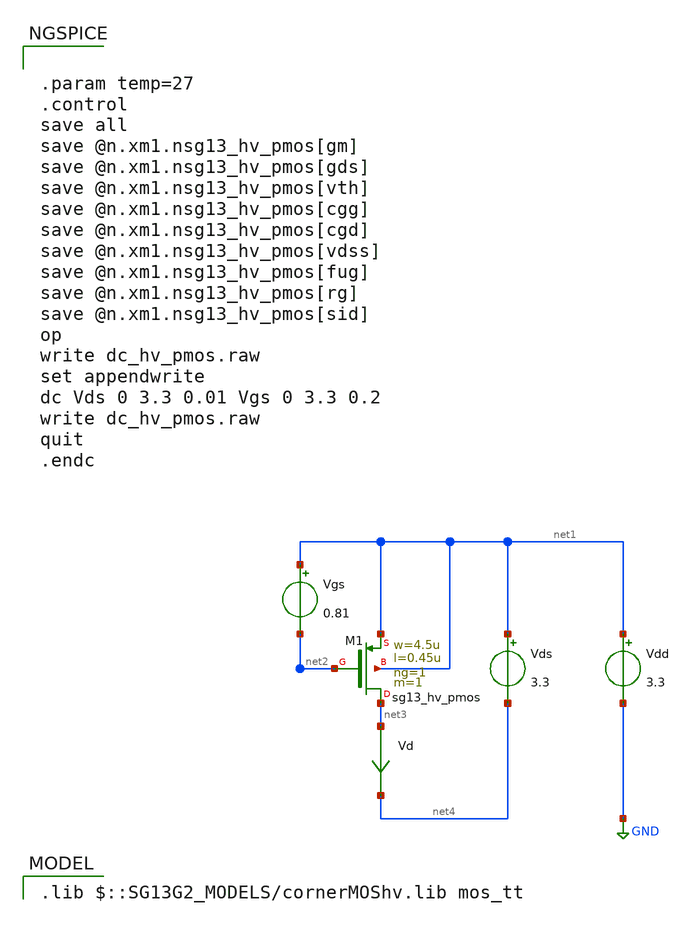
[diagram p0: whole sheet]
** sch_path: xschem/dc_hv_pmos.sch
* Copyright 2023-2024 IHP PDK Authors, Harald Pretl
**.subckt dc_hv_pmos
Vgs net1 net2 0.81
Vds net1 net4 3.3
Vd net3 net4 0
.save i(vd)
Vdd net1 GND 3.3
XM1 net3 net2 net1 net1 sg13_hv_pmos w=4.5u l=0.45u ng=1 m=1 mm_ok=1
**** begin user architecture code
 .lib $::SG13G2_MODELS/cornerMOShv.lib mos_tt



.param temp=27
.control
save all
save @n.xm1.nsg13_hv_pmos[gm]
save @n.xm1.nsg13_hv_pmos[gds]
save @n.xm1.nsg13_hv_pmos[vth]
save @n.xm1.nsg13_hv_pmos[cgg]
save @n.xm1.nsg13_hv_pmos[cgd]
save @n.xm1.nsg13_hv_pmos[vdss]
save @n.xm1.nsg13_hv_pmos[fug]
save @n.xm1.nsg13_hv_pmos[rg]
save @n.xm1.nsg13_hv_pmos[sid]
op
write dc_hv_pmos.raw
set appendwrite
dc Vds 0 3.3 0.01 Vgs 0 3.3 0.2
write dc_hv_pmos.raw
quit
.endc


**** end user architecture code
**.ends
.GLOBAL GND
.end
